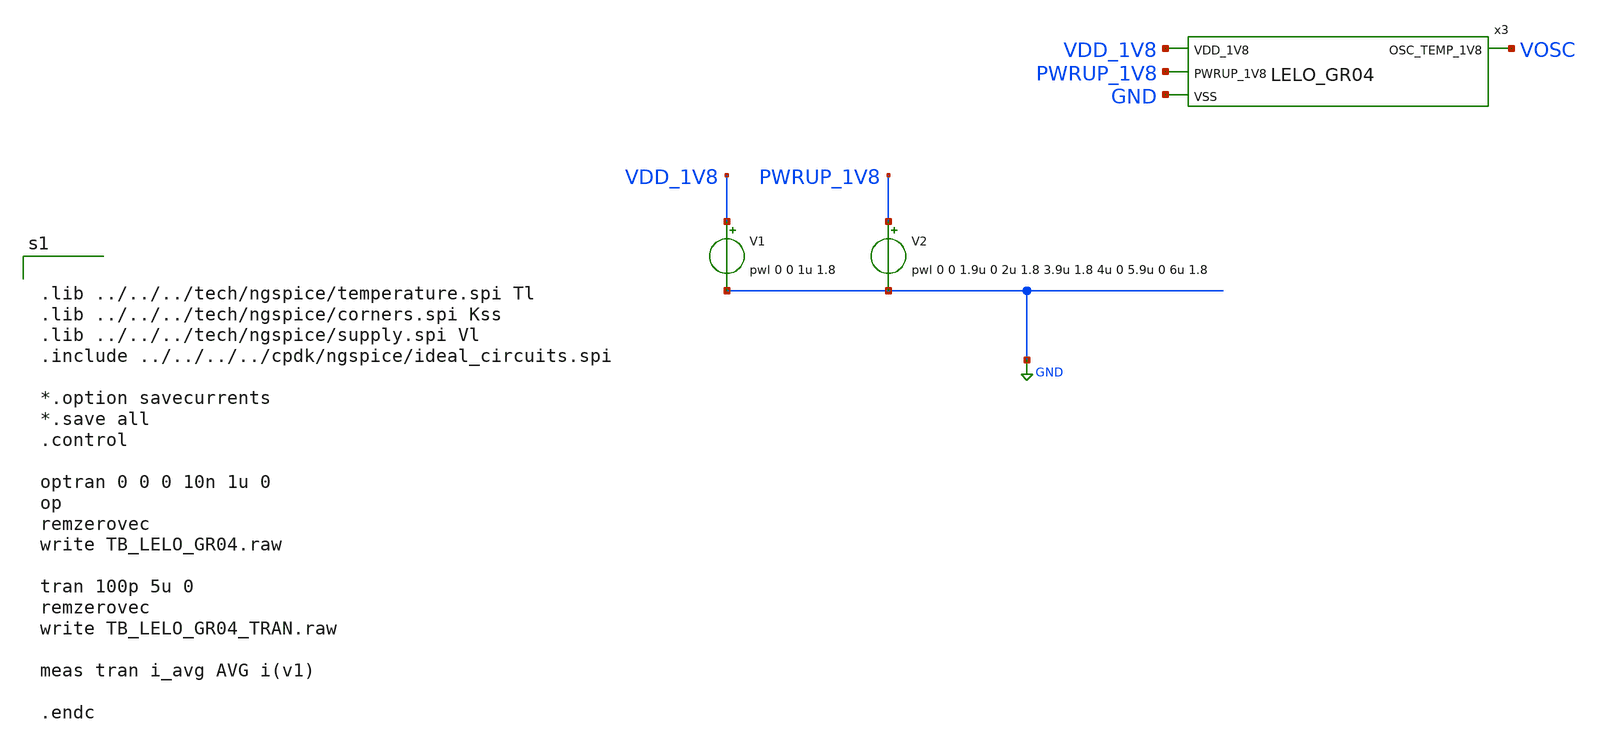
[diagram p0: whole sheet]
** sch_path: design/LELO_GR04_SKY130A/TB_LELO_GR04.sch
**.subckt TB_LELO_GR04
V1 VDD_1V8 GND pwl 0 0 1u 1.8
V2 PWRUP_1V8 GND pwl 0 0 1.9u 0 2u 1.8 3.9u 1.8 4u 0 5.9u 0 6u 1.8
x3 VDD_1V8 VOSC PWRUP_1V8 GND LELO_GR04
**** begin user architecture code


.lib ../../../tech/ngspice/temperature.spi Tl
.lib ../../../tech/ngspice/corners.spi Kss
.lib ../../../tech/ngspice/supply.spi Vl
.include ../../../../cpdk/ngspice/ideal_circuits.spi

*.option savecurrents
*.save all
.control

optran 0 0 0 10n 1u 0
op
remzerovec
write TB_LELO_GR04.raw

tran 100p 5u 0
remzerovec
write TB_LELO_GR04_TRAN.raw

meas tran i_avg AVG i(v1)

.endc


**** end user architecture code
**.ends
.GLOBAL GND
.end
